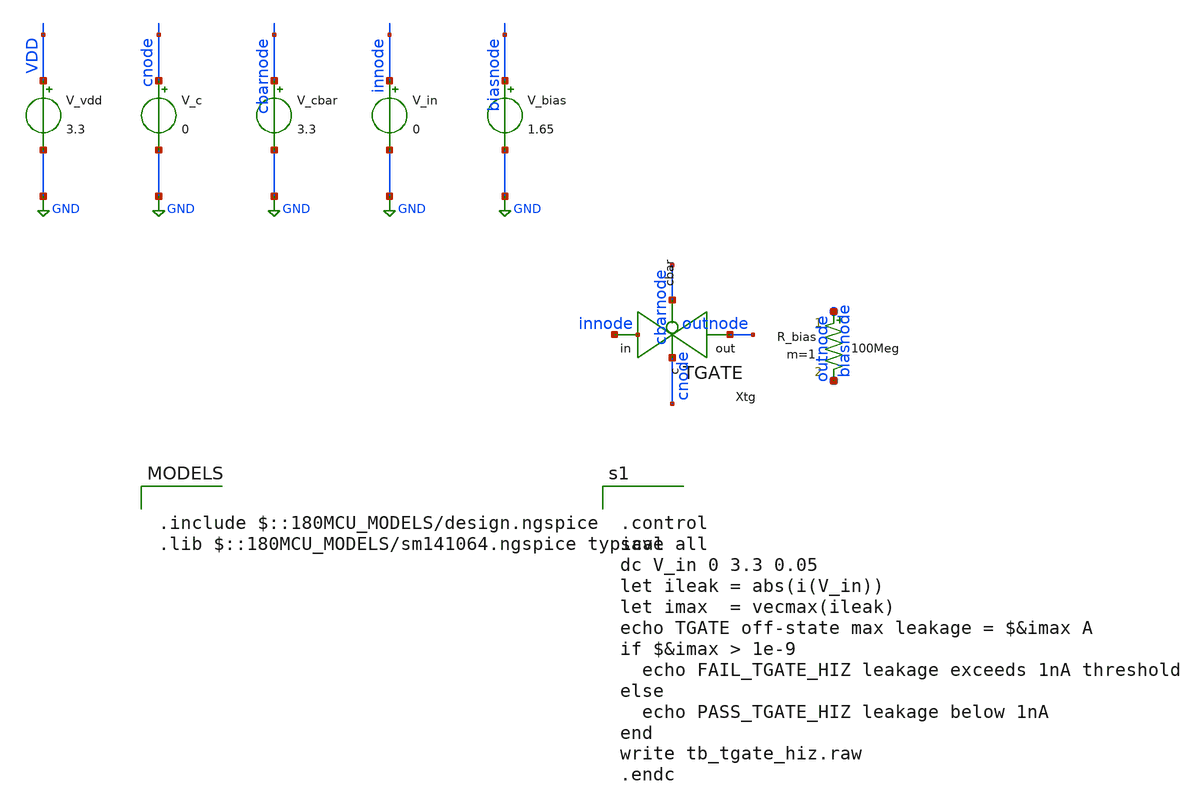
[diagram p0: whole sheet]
** sch_path: tb_tgate_hiz.sch
**.subckt tb_tgate_hiz
V_vdd VDD GND 3.3
V_c cnode GND 0
V_cbar cbarnode GND 3.3
V_in innode GND 0
.save i(v_in)
V_bias biasnode GND 1.65
Xtg outnode cnode cbarnode innode TGATE
R_bias outnode biasnode 100Meg m=1
**** begin user architecture code

.include $::180MCU_MODELS/design.ngspice
.lib $::180MCU_MODELS/sm141064.ngspice typical



.control
save all
dc V_in 0 3.3 0.05
let ileak = abs(i(V_in))
let imax  = vecmax(ileak)
echo TGATE off-state max leakage = $&imax A
if $&imax > 1e-9
  echo FAIL_TGATE_HIZ leakage exceeds 1nA threshold
else
  echo PASS_TGATE_HIZ leakage below 1nA
end
write tb_tgate_hiz.raw
.endc


**** end user architecture code
**.ends

* expanding   symbol:  TGATE/TGATE.sym # of pins=4
** sym_path: TGATE/TGATE.sym
** sch_path: TGATE/TGATE.sch
.subckt TGATE out c cbar in
*.ipin in
*.opin out
*.ipin cbar
*.ipin c
XM1 out cbar in VDD pfet_03v3 L=0.28u W=1u nf=1 ad='int((nf+1)/2) * W/nf * 0.18u' as='int((nf+2)/2) * W/nf * 0.18u'
+ pd='2*int((nf+1)/2) * (W/nf + 0.18u)' ps='2*int((nf+2)/2) * (W/nf + 0.18u)' nrd='0.18u / W' nrs='0.18u / W'
+ sa=0 sb=0 sd=0 m=1
XM2 out c in GND nfet_03v3 L=0.28u W=1u nf=1 ad='int((nf+1)/2) * W/nf * 0.18u' as='int((nf+2)/2) * W/nf * 0.18u'
+ pd='2*int((nf+1)/2) * (W/nf + 0.18u)' ps='2*int((nf+2)/2) * (W/nf + 0.18u)' nrd='0.18u / W' nrs='0.18u / W'
+ sa=0 sb=0 sd=0 m=1
.ends

.GLOBAL GND
.GLOBAL VDD
.end
